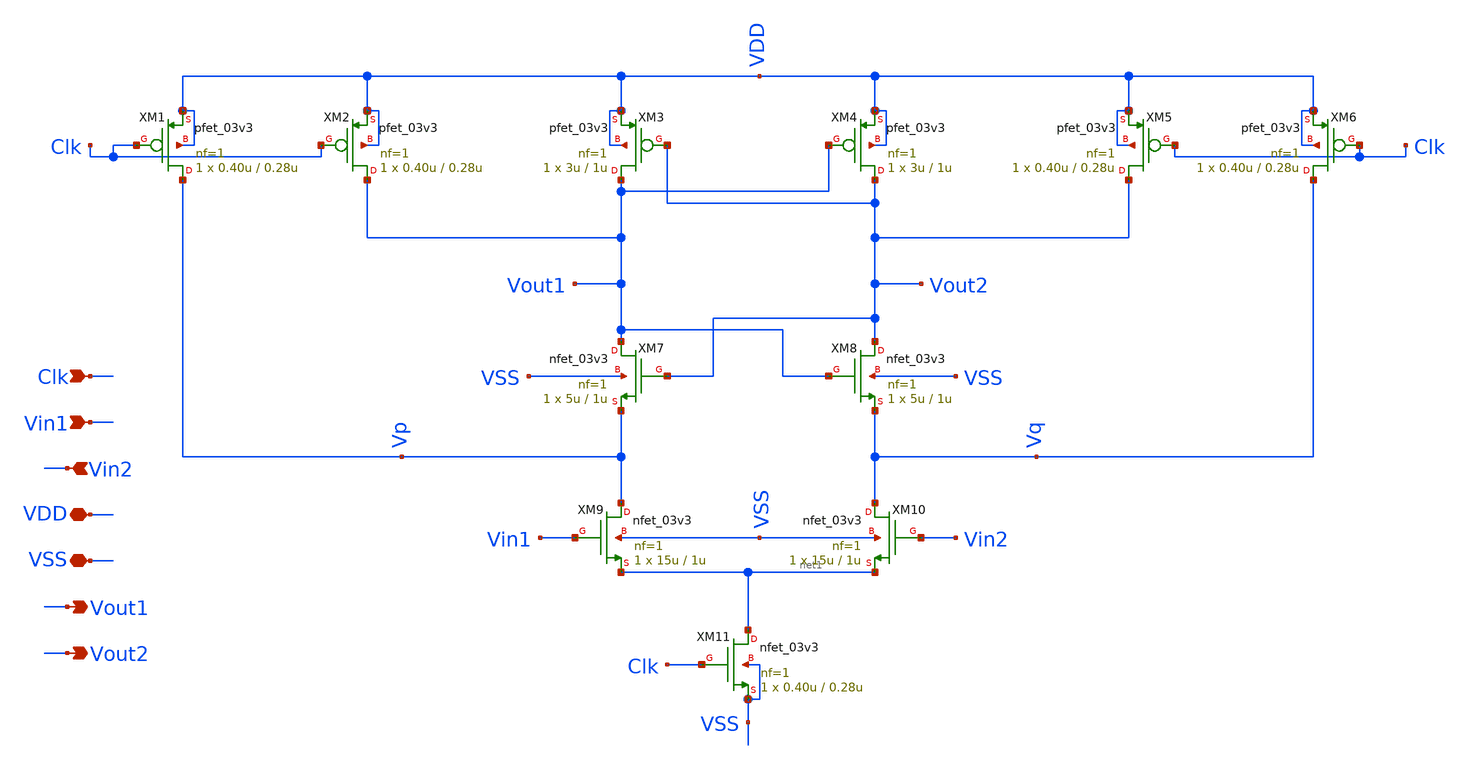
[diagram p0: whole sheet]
** sch_path: Analog/schematics/comparator/strongArmLatch.sch
**.subckt strongArmLatch Clk Vin1 Vin2 VDD VSS Vout1 Vout2
*.ipin Clk
*.ipin Vin1
*.ipin Vin2
*.iopin VDD
*.iopin VSS
*.opin Vout1
*.opin Vout2
XM1 Vp Clk VDD VDD pfet_03v3 L=0.28u W=0.40u nf=1 ad='int((nf+1)/2) * W/nf * 0.18u' as='int((nf+2)/2) * W/nf * 0.18u'
+ pd='2*int((nf+1)/2) * (W/nf + 0.18u)' ps='2*int((nf+2)/2) * (W/nf + 0.18u)' nrd='0.18u / W' nrs='0.18u / W'
+ sa=0 sb=0 sd=0 m=1
XM2 Vout1 Clk VDD VDD pfet_03v3 L=0.28u W=0.40u nf=1 ad='int((nf+1)/2) * W/nf * 0.18u' as='int((nf+2)/2) * W/nf * 0.18u'
+ pd='2*int((nf+1)/2) * (W/nf + 0.18u)' ps='2*int((nf+2)/2) * (W/nf + 0.18u)' nrd='0.18u / W' nrs='0.18u / W'
+ sa=0 sb=0 sd=0 m=1
XM3 Vout1 Vout2 VDD VDD pfet_03v3 L=1u W=3u nf=1 ad='int((nf+1)/2) * W/nf * 0.18u' as='int((nf+2)/2) * W/nf * 0.18u'
+ pd='2*int((nf+1)/2) * (W/nf + 0.18u)' ps='2*int((nf+2)/2) * (W/nf + 0.18u)' nrd='0.18u / W' nrs='0.18u / W'
+ sa=0 sb=0 sd=0 m=1
XM4 Vout2 Vout1 VDD VDD pfet_03v3 L=1u W=3u nf=1 ad='int((nf+1)/2) * W/nf * 0.18u' as='int((nf+2)/2) * W/nf * 0.18u'
+ pd='2*int((nf+1)/2) * (W/nf + 0.18u)' ps='2*int((nf+2)/2) * (W/nf + 0.18u)' nrd='0.18u / W' nrs='0.18u / W'
+ sa=0 sb=0 sd=0 m=1
XM5 Vout2 Clk VDD VDD pfet_03v3 L=0.28u W=0.40u nf=1 ad='int((nf+1)/2) * W/nf * 0.18u' as='int((nf+2)/2) * W/nf * 0.18u'
+ pd='2*int((nf+1)/2) * (W/nf + 0.18u)' ps='2*int((nf+2)/2) * (W/nf + 0.18u)' nrd='0.18u / W' nrs='0.18u / W'
+ sa=0 sb=0 sd=0 m=1
XM6 Vq Clk VDD VDD pfet_03v3 L=0.28u W=0.40u nf=1 ad='int((nf+1)/2) * W/nf * 0.18u' as='int((nf+2)/2) * W/nf * 0.18u'
+ pd='2*int((nf+1)/2) * (W/nf + 0.18u)' ps='2*int((nf+2)/2) * (W/nf + 0.18u)' nrd='0.18u / W' nrs='0.18u / W'
+ sa=0 sb=0 sd=0 m=1
XM7 Vout1 Vout2 Vp VSS nfet_03v3 L=1u W=5u nf=1 ad='int((nf+1)/2) * W/nf * 0.18u' as='int((nf+2)/2) * W/nf * 0.18u'
+ pd='2*int((nf+1)/2) * (W/nf + 0.18u)' ps='2*int((nf+2)/2) * (W/nf + 0.18u)' nrd='0.18u / W' nrs='0.18u / W'
+ sa=0 sb=0 sd=0 m=1
XM8 Vout2 Vout1 Vq VSS nfet_03v3 L=1u W=5u nf=1 ad='int((nf+1)/2) * W/nf * 0.18u' as='int((nf+2)/2) * W/nf * 0.18u'
+ pd='2*int((nf+1)/2) * (W/nf + 0.18u)' ps='2*int((nf+2)/2) * (W/nf + 0.18u)' nrd='0.18u / W' nrs='0.18u / W'
+ sa=0 sb=0 sd=0 m=1
XM9 Vp Vin1 net1 VSS nfet_03v3 L=1u W=15u nf=1 ad='int((nf+1)/2) * W/nf * 0.18u' as='int((nf+2)/2) * W/nf * 0.18u'
+ pd='2*int((nf+1)/2) * (W/nf + 0.18u)' ps='2*int((nf+2)/2) * (W/nf + 0.18u)' nrd='0.18u / W' nrs='0.18u / W'
+ sa=0 sb=0 sd=0 m=1
XM10 Vq Vin2 net1 VSS nfet_03v3 L=1u W=15u nf=1 ad='int((nf+1)/2) * W/nf * 0.18u' as='int((nf+2)/2) * W/nf * 0.18u'
+ pd='2*int((nf+1)/2) * (W/nf + 0.18u)' ps='2*int((nf+2)/2) * (W/nf + 0.18u)' nrd='0.18u / W' nrs='0.18u / W'
+ sa=0 sb=0 sd=0 m=1
XM11 net1 Clk VSS VSS nfet_03v3 L=0.28u W=0.40u nf=1 ad='int((nf+1)/2) * W/nf * 0.18u' as='int((nf+2)/2) * W/nf * 0.18u'
+ pd='2*int((nf+1)/2) * (W/nf + 0.18u)' ps='2*int((nf+2)/2) * (W/nf + 0.18u)' nrd='0.18u / W' nrs='0.18u / W'
+ sa=0 sb=0 sd=0 m=1
**.ends
.end
